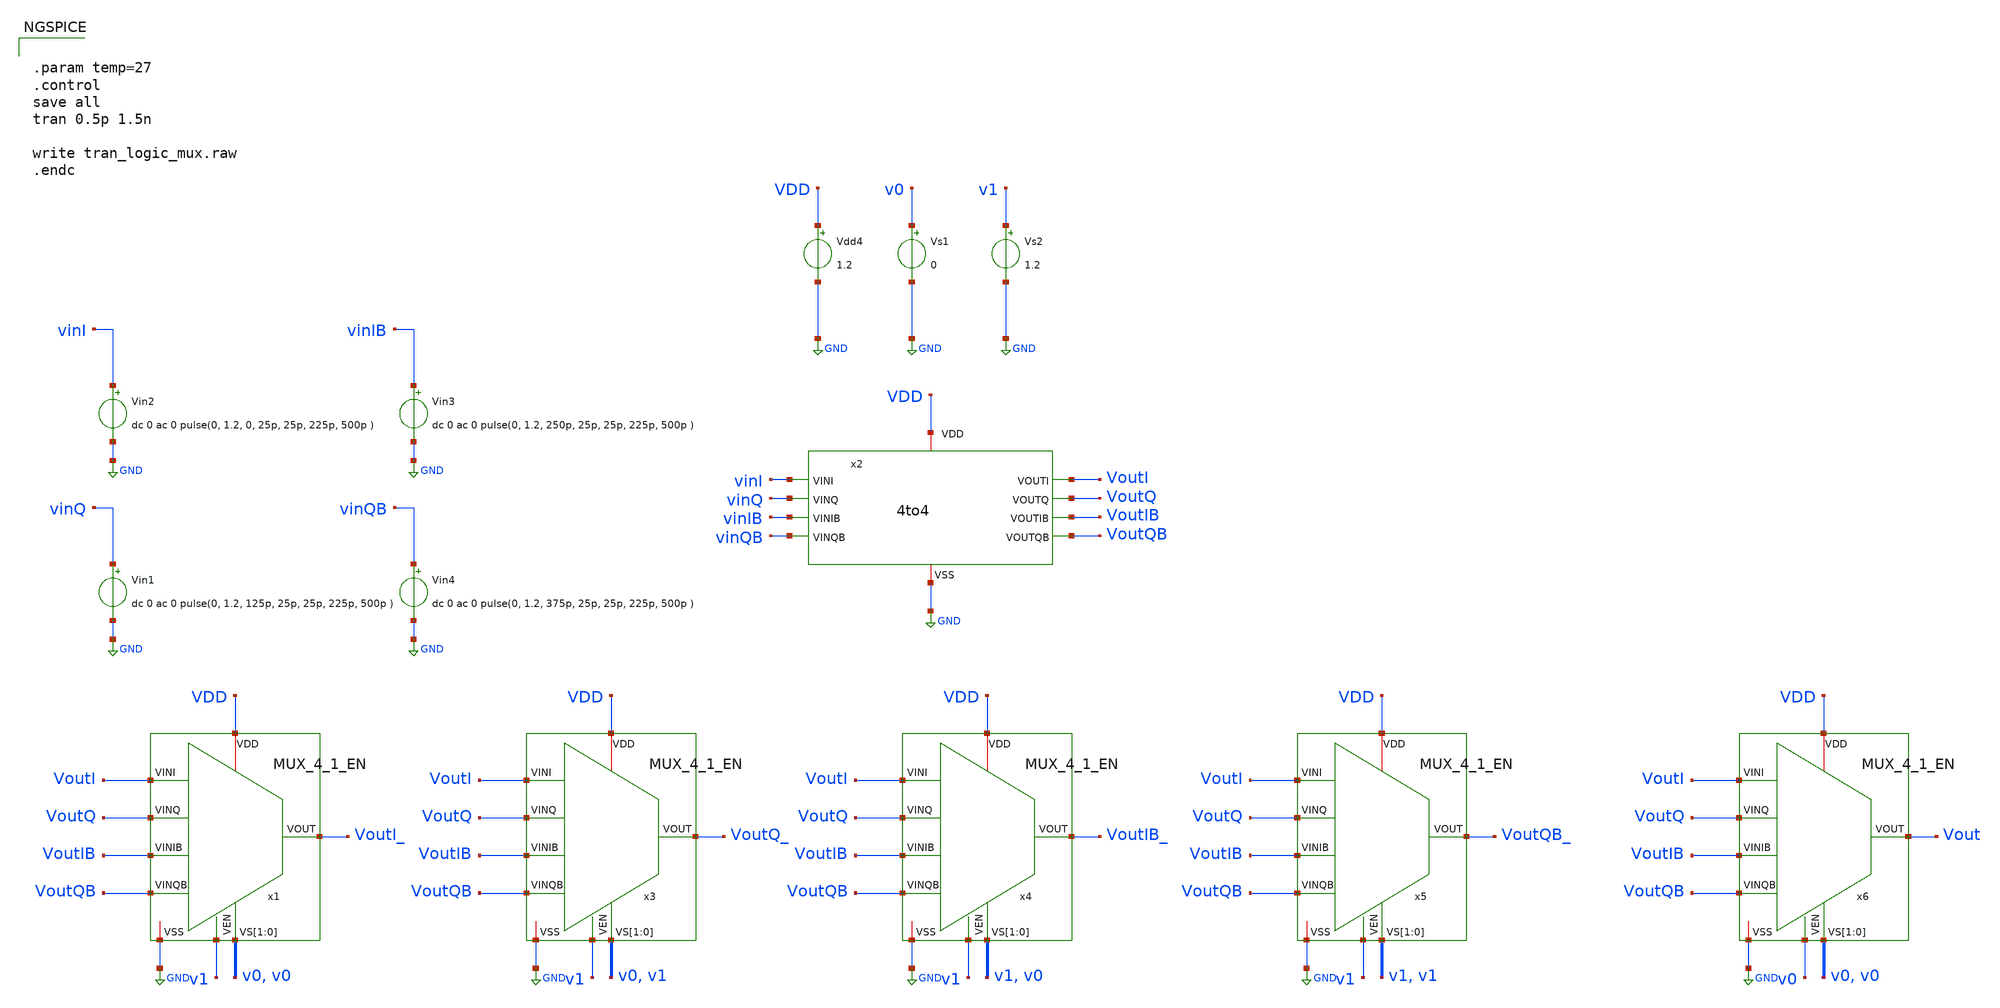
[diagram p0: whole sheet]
** sch_path: tb_MUX_4_1.sch
**.subckt tb_MUX_4_1
Vdd4 VDD GND 1.2
Vin2 vinI GND dc 0 ac 0 pulse(0, 1.2, 0, 25p, 25p, 225p, 500p )
Vin1 vinQ GND dc 0 ac 0 pulse(0, 1.2, 125p, 25p, 25p, 225p, 500p )
Vs2 v1 GND 1.2
Vs1 v0 GND 0
Vin3 vinIB GND dc 0 ac 0 pulse(0, 1.2, 250p, 25p, 25p, 225p, 500p )
Vin4 vinQB GND dc 0 ac 0 pulse(0, 1.2, 375p, 25p, 25p, 225p, 500p )
x2 VDD vinI VoutI VoutQ vinQ vinIB VoutIB vinQB VoutQB GND 4to4
x1 v1 VoutI VoutQ VDD VoutI_ v0 v0 VoutIB GND VoutQB MUX_4_1_EN
x3 v1 VoutI VoutQ VDD VoutQ_ v0 v1 VoutIB GND VoutQB MUX_4_1_EN
x4 v1 VoutI VoutQ VDD VoutIB_ v1 v0 VoutIB GND VoutQB MUX_4_1_EN
x5 v1 VoutI VoutQ VDD VoutQB_ v1 v1 VoutIB GND VoutQB MUX_4_1_EN
x6 v0 VoutI VoutQ VDD Vout v0 v0 VoutIB GND VoutQB MUX_4_1_EN
**** begin user architecture code


.param temp=27
.control
save all
tran 0.5p 1.5n

write tran_logic_mux.raw
.endc



.lib cornerMOSlv.lib mos_tt

**** end user architecture code
**.ends
.GLOBAL GND
.end
